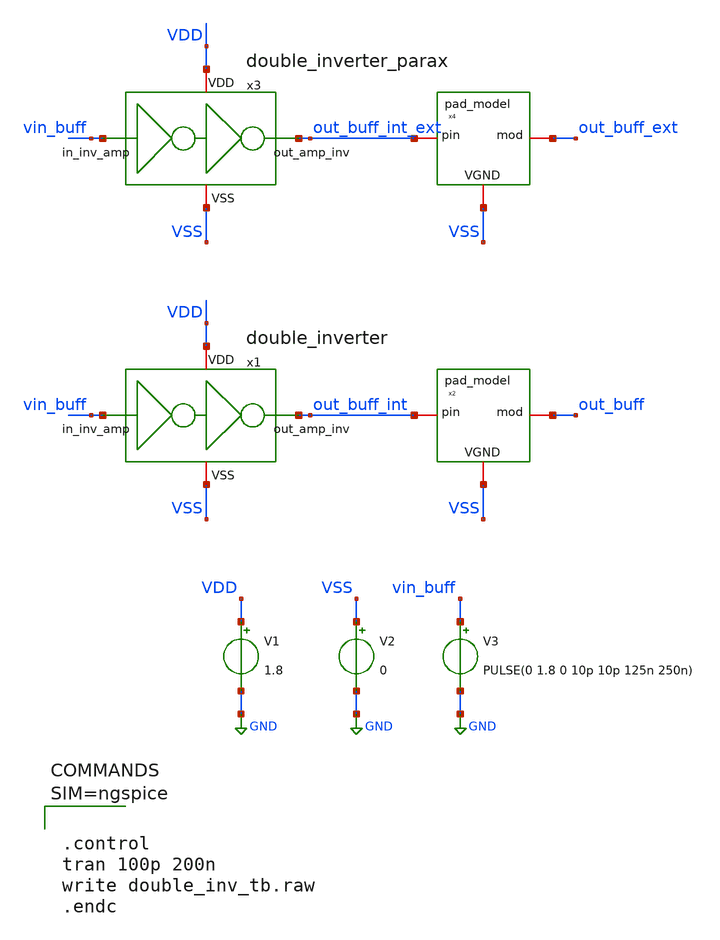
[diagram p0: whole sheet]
** sch_path: xschem/double_inv_tb.sch
**.subckt double_inv_tb
V1 VDD GND 1.8
V2 VSS GND 0
x1 VDD VSS out_buff_int vin_buff double_inverter
x2 VSS out_buff_int out_buff pad_model
V3 vin_buff GND PULSE(0 1.8 0 10p 10p 125n 250n)
x3 VDD VSS out_buff_int_ext vin_buff double_inverter_parax
x4 VSS out_buff_int_ext out_buff_ext pad_model
**** begin user architecture code

** opencircuitdesign pdks install
.lib $::SKYWATER_MODELS/sky130.lib.spice tt





.control
tran 100p 200n
write double_inv_tb.raw
.endc



**** end user architecture code
**.ends
.GLOBAL GND
.end
